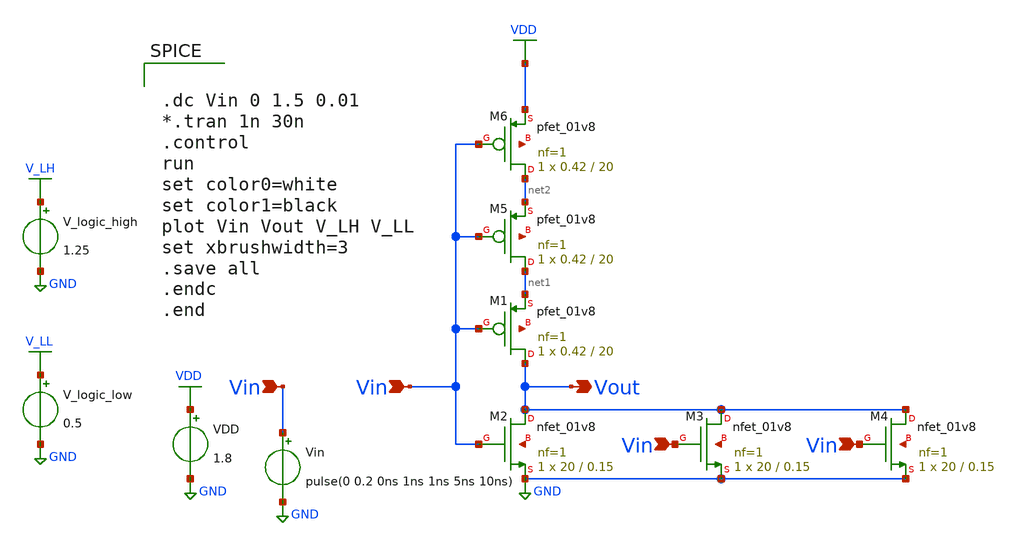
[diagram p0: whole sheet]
** sch_path: xschem/DC_Analysis_Inverter-test.sch
**.subckt DC_Analysis_Inverter-test Vin Vin Vout Vin Vin
*.ipin Vin
*.ipin Vin
*.opin Vout
*.ipin Vin
*.ipin Vin
VDD VDD GND 1.8
Vin Vin GND pulse(0 0.2 0ns 1ns 1ns 5ns 10ns)
XM1 Vout Vin net1 net3 sky130_fd_pr__pfet_01v8 L=20 W=0.42 nf=1 ad='int((nf+1)/2) * W/nf * 0.29' as='int((nf+2)/2) * W/nf * 0.29'
+ pd='2*int((nf+1)/2) * (W/nf + 0.29)' ps='2*int((nf+2)/2) * (W/nf + 0.29)' nrd='0.29 / W' nrs='0.29 / W'
+ sa=0 sb=0 sd=0 mult=1 m=1
XM2 Vout Vin GND net4 sky130_fd_pr__nfet_01v8 L=0.15 W=20 nf=1 ad='int((nf+1)/2) * W/nf * 0.29' as='int((nf+2)/2) * W/nf * 0.29'
+ pd='2*int((nf+1)/2) * (W/nf + 0.29)' ps='2*int((nf+2)/2) * (W/nf + 0.29)' nrd='0.29 / W' nrs='0.29 / W'
+ sa=0 sb=0 sd=0 mult=1 m=1
V_logic_high V_LH GND 1.25
V_logic_low V_LL GND 0.5
XM3 Vout Vin GND net5 sky130_fd_pr__nfet_01v8 L=0.15 W=20 nf=1 ad='int((nf+1)/2) * W/nf * 0.29' as='int((nf+2)/2) * W/nf * 0.29'
+ pd='2*int((nf+1)/2) * (W/nf + 0.29)' ps='2*int((nf+2)/2) * (W/nf + 0.29)' nrd='0.29 / W' nrs='0.29 / W'
+ sa=0 sb=0 sd=0 mult=1 m=1
XM4 Vout Vin GND net6 sky130_fd_pr__nfet_01v8 L=0.15 W=20 nf=1 ad='int((nf+1)/2) * W/nf * 0.29' as='int((nf+2)/2) * W/nf * 0.29'
+ pd='2*int((nf+1)/2) * (W/nf + 0.29)' ps='2*int((nf+2)/2) * (W/nf + 0.29)' nrd='0.29 / W' nrs='0.29 / W'
+ sa=0 sb=0 sd=0 mult=1 m=1
XM5 net1 Vin net2 net7 sky130_fd_pr__pfet_01v8 L=20 W=0.42 nf=1 ad='int((nf+1)/2) * W/nf * 0.29' as='int((nf+2)/2) * W/nf * 0.29'
+ pd='2*int((nf+1)/2) * (W/nf + 0.29)' ps='2*int((nf+2)/2) * (W/nf + 0.29)' nrd='0.29 / W' nrs='0.29 / W'
+ sa=0 sb=0 sd=0 mult=1 m=1
XM6 net2 Vin VDD net8 sky130_fd_pr__pfet_01v8 L=20 W=0.42 nf=1 ad='int((nf+1)/2) * W/nf * 0.29' as='int((nf+2)/2) * W/nf * 0.29'
+ pd='2*int((nf+1)/2) * (W/nf + 0.29)' ps='2*int((nf+2)/2) * (W/nf + 0.29)' nrd='0.29 / W' nrs='0.29 / W'
+ sa=0 sb=0 sd=0 mult=1 m=1
**** begin user architecture code


.dc Vin 0 1.5 0.01
*.tran 1n 30n
.control
run
set color0=white
set color1=black
plot Vin Vout V_LH V_LL
set xbrushwidth=3
.save all
.endc
.end




.lib /usr/local/share/pdk/sky130A/libs.tech/ngspice/sky130.lib.spice tt

.save all



**** end user architecture code
**.ends
.GLOBAL VDD
.GLOBAL GND
.GLOBAL V_LH
.GLOBAL V_LL
.end
